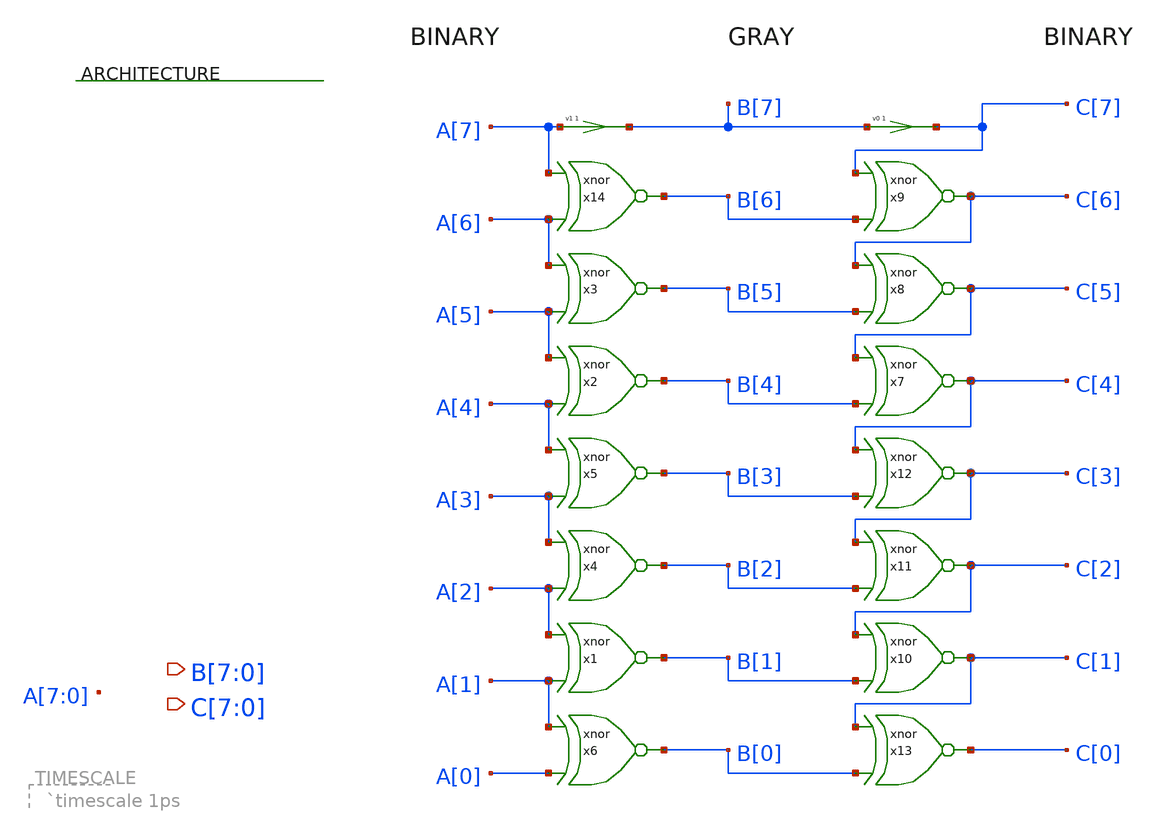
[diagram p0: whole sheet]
** sch_path: library/examples/greycnt.sch
**.subckt greycnt B[7],B[6],B[5],B[4],B[3],B[2],B[1],B[0] C[7],C[6],C[5],C[4],C[3],C[2],C[1],C[0]
*.opin B[7],B[6],B[5],B[4],B[3],B[2],B[1],B[0]
*.opin C[7],C[6],C[5],C[4],C[3],C[2],C[1],C[0]
v1 B[7] A[7] 0
v0 C[7] B[7] 0
**.ends
.end
